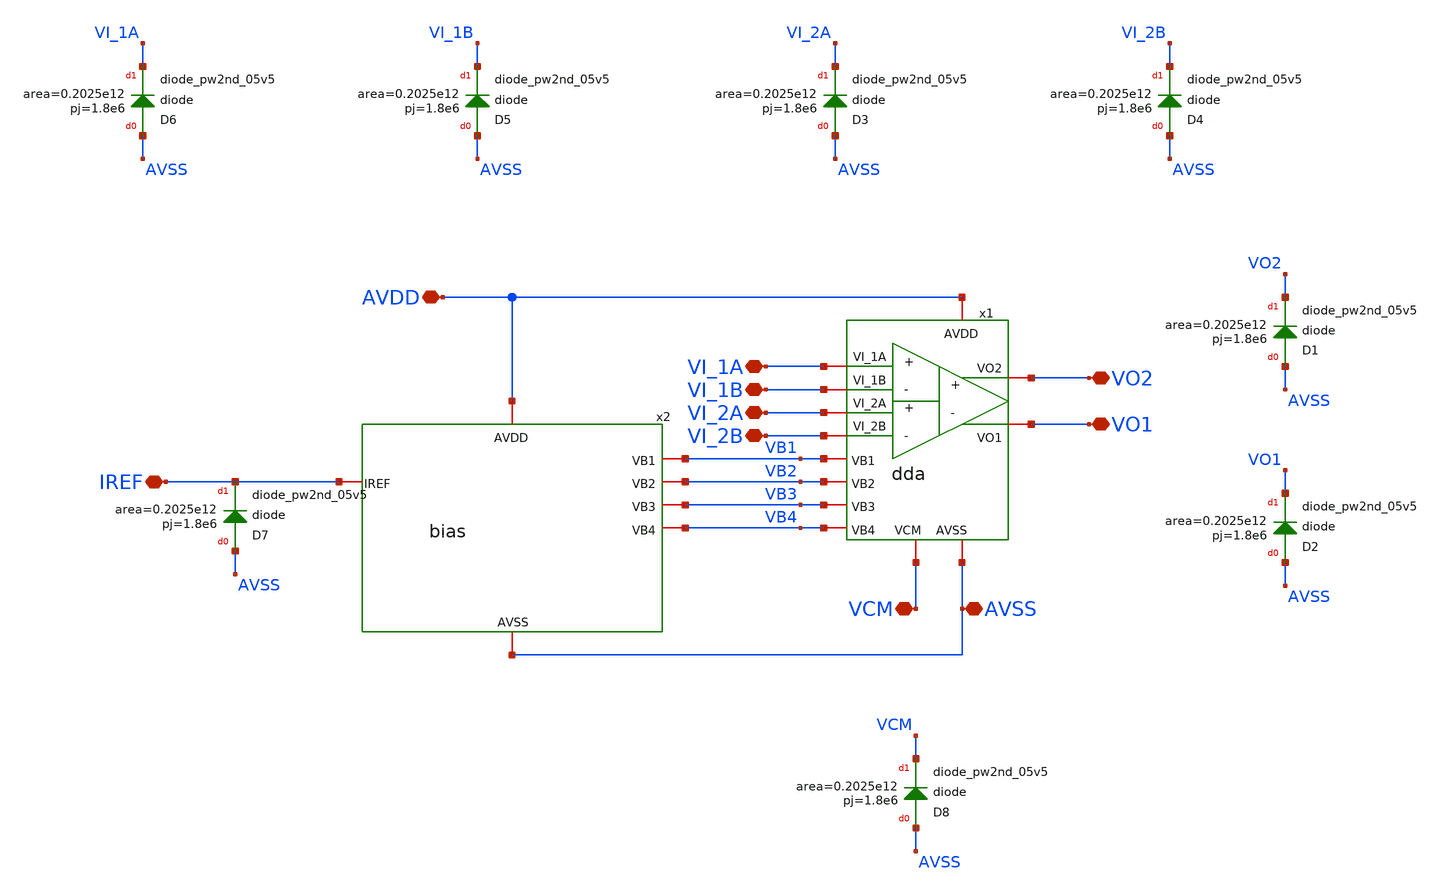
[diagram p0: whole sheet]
** sch_path: xschem/INA_layout_v2/ina_top.sch
**.subckt ina_top IREF VI_1A VI_1B VI_2A VI_2B VO2 VO1 VCM AVDD AVSS
*.iopin IREF
*.iopin VI_1A
*.iopin VI_1B
*.iopin VI_2A
*.iopin VI_2B
*.iopin VO2
*.iopin VO1
*.iopin VCM
*.iopin AVDD
*.iopin AVSS
x1 AVDD AVSS VI_1A VI_1B VO2 VO1 VCM VB1 VB2 VB3 VB4 VI_2A VI_2B dda
x2 IREF VB1 AVDD AVSS VB2 VB3 VB4 bias
XD3 AVSS VI_2A sky130_fd_pr__diode_pw2nd_05v5 area=0.2025e12 pj=1.8e6
XD4 AVSS VI_2B sky130_fd_pr__diode_pw2nd_05v5 area=0.2025e12 pj=1.8e6
XD5 AVSS VI_1B sky130_fd_pr__diode_pw2nd_05v5 area=0.2025e12 pj=1.8e6
XD6 AVSS VI_1A sky130_fd_pr__diode_pw2nd_05v5 area=0.2025e12 pj=1.8e6
XD7 AVSS IREF sky130_fd_pr__diode_pw2nd_05v5 area=0.2025e12 pj=1.8e6
XD2 AVSS VO1 sky130_fd_pr__diode_pw2nd_05v5 area=0.2025e12 pj=1.8e6
XD1 AVSS VO2 sky130_fd_pr__diode_pw2nd_05v5 area=0.2025e12 pj=1.8e6
XD8 AVSS VCM sky130_fd_pr__diode_pw2nd_05v5 area=0.2025e12 pj=1.8e6
**.ends
.end
